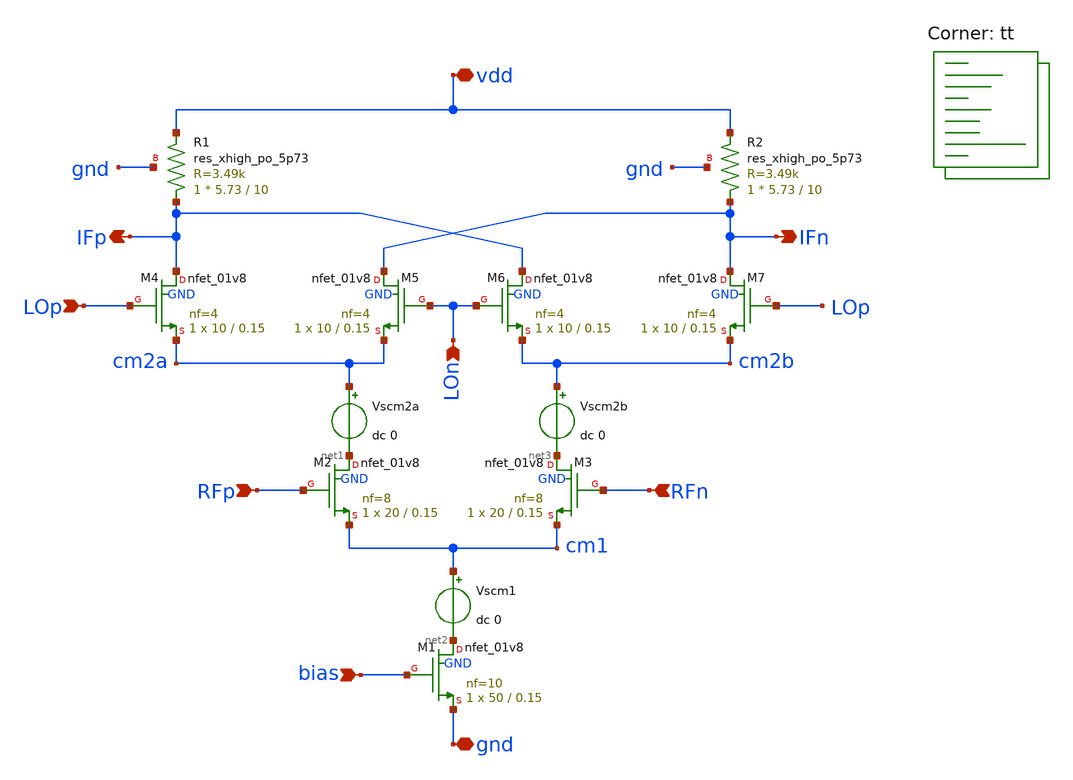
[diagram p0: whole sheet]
** sch_path: xschem/mixer_final.sch
**.subckt mixer_final LOp RFp RFn LOn bias gnd vdd IFp IFn
*.ipin LOp
*.ipin RFp
*.ipin RFn
*.ipin LOn
*.ipin bias
*.iopin gnd
*.iopin vdd
*.opin IFp
*.opin IFn
XM2 net1 RFp cm1 GND sky130_fd_pr__nfet_01v8 L=0.15 W=20 nf=8 ad='int((nf+1)/2) * W/nf * 0.29' as='int((nf+2)/2) * W/nf * 0.29'
+ pd='2*int((nf+1)/2) * (W/nf + 0.29)' ps='2*int((nf+2)/2) * (W/nf + 0.29)' nrd='0.29 / W' nrs='0.29 / W'
+ sa=0 sb=0 sd=0 mult=1 m=1
XM1 net2 bias gnd GND sky130_fd_pr__nfet_01v8 L=0.15 W=50 nf=10 ad='int((nf+1)/2) * W/nf * 0.29' as='int((nf+2)/2) * W/nf * 0.29'
+ pd='2*int((nf+1)/2) * (W/nf + 0.29)' ps='2*int((nf+2)/2) * (W/nf + 0.29)' nrd='0.29 / W' nrs='0.29 / W'
+ sa=0 sb=0 sd=0 mult=1 m=1
XM3 net3 RFn cm1 GND sky130_fd_pr__nfet_01v8 L=0.15 W=20 nf=8 ad='int((nf+1)/2) * W/nf * 0.29' as='int((nf+2)/2) * W/nf * 0.29'
+ pd='2*int((nf+1)/2) * (W/nf + 0.29)' ps='2*int((nf+2)/2) * (W/nf + 0.29)' nrd='0.29 / W' nrs='0.29 / W'
+ sa=0 sb=0 sd=0 mult=1 m=1
XM4 IFp LOp cm2a GND sky130_fd_pr__nfet_01v8 L=0.15 W=10 nf=4 ad='int((nf+1)/2) * W/nf * 0.29' as='int((nf+2)/2) * W/nf * 0.29'
+ pd='2*int((nf+1)/2) * (W/nf + 0.29)' ps='2*int((nf+2)/2) * (W/nf + 0.29)' nrd='0.29 / W' nrs='0.29 / W'
+ sa=0 sb=0 sd=0 mult=1 m=1
XM5 IFn LOn cm2a GND sky130_fd_pr__nfet_01v8 L=0.15 W=10 nf=4 ad='int((nf+1)/2) * W/nf * 0.29' as='int((nf+2)/2) * W/nf * 0.29'
+ pd='2*int((nf+1)/2) * (W/nf + 0.29)' ps='2*int((nf+2)/2) * (W/nf + 0.29)' nrd='0.29 / W' nrs='0.29 / W'
+ sa=0 sb=0 sd=0 mult=1 m=1
XM6 IFp LOn cm2b GND sky130_fd_pr__nfet_01v8 L=0.15 W=10 nf=4 ad='int((nf+1)/2) * W/nf * 0.29' as='int((nf+2)/2) * W/nf * 0.29'
+ pd='2*int((nf+1)/2) * (W/nf + 0.29)' ps='2*int((nf+2)/2) * (W/nf + 0.29)' nrd='0.29 / W' nrs='0.29 / W'
+ sa=0 sb=0 sd=0 mult=1 m=1
XM7 IFn LOp cm2b GND sky130_fd_pr__nfet_01v8 L=0.15 W=10 nf=4 ad='int((nf+1)/2) * W/nf * 0.29' as='int((nf+2)/2) * W/nf * 0.29'
+ pd='2*int((nf+1)/2) * (W/nf + 0.29)' ps='2*int((nf+2)/2) * (W/nf + 0.29)' nrd='0.29 / W' nrs='0.29 / W'
+ sa=0 sb=0 sd=0 mult=1 m=1
Vscm1 cm1 net2 dc 0
Vscm2b cm2b net3 dc 0
Vscm2a cm2a net1 dc 0
XR1 IFp vdd gnd sky130_fd_pr__res_xhigh_po_5p73 L=10 mult=1 m=1
XR2 IFn vdd gnd sky130_fd_pr__res_xhigh_po_5p73 L=10 mult=1 m=1
**** begin user architecture code
.lib $::SKYWATER_MODELS/sky130.lib.spice tt
**** end user architecture code
**.ends
.end
